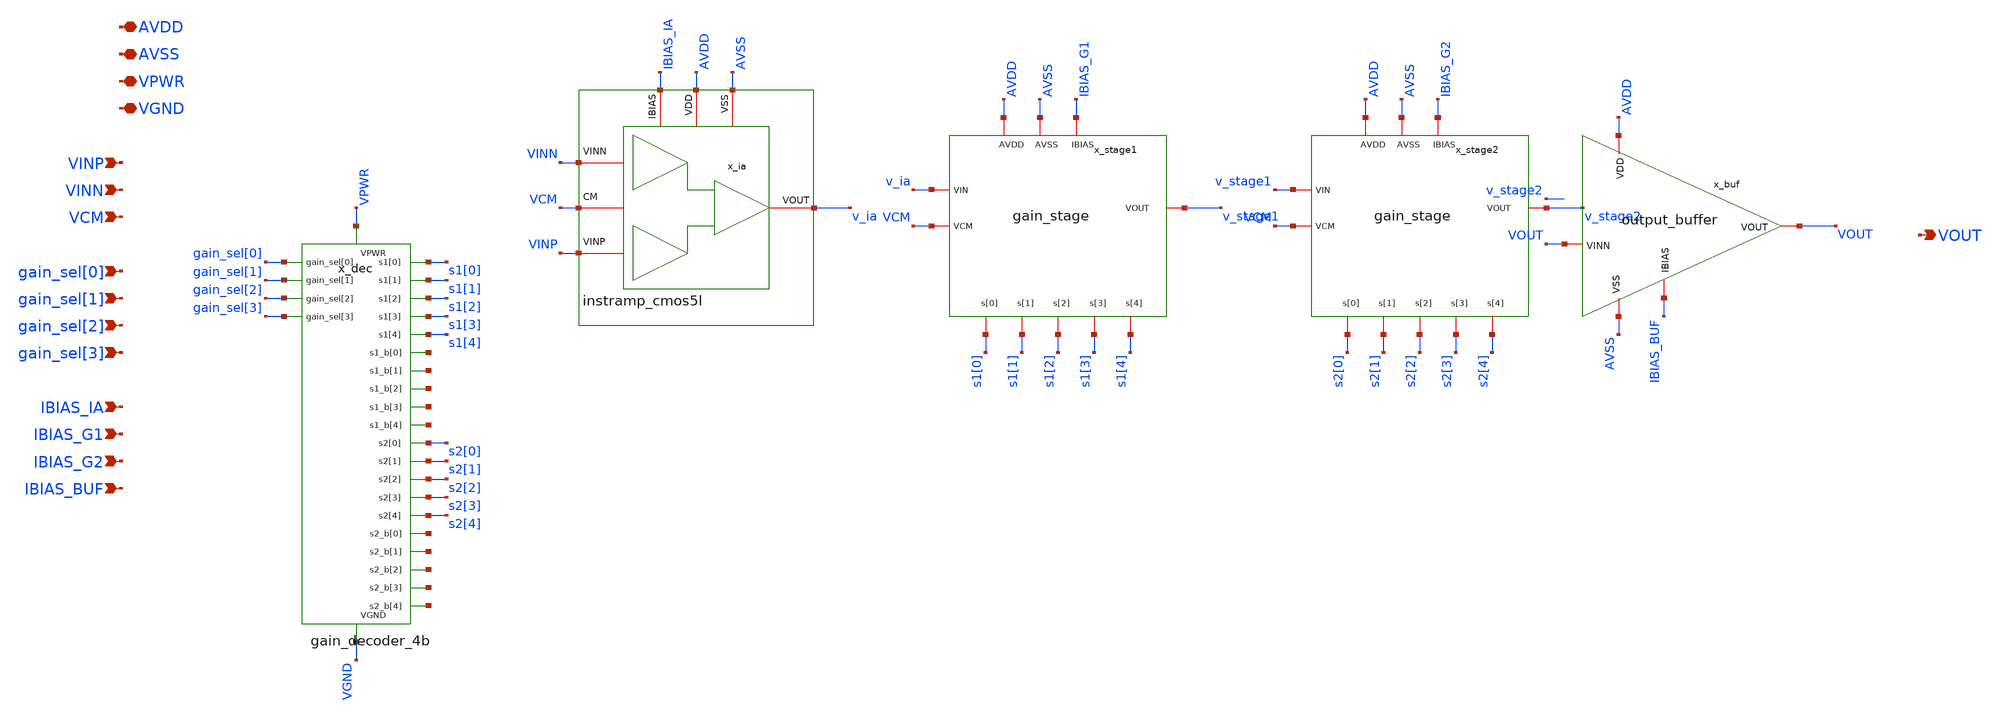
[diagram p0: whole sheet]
** sch_path: xschem/pgia_top/pgia_top.sch
**.subckt pgia_top AVDD AVSS VPWR VGND VINP VINN VCM gain_sel[0] gain_sel[1] gain_sel[2] gain_sel[3]
*+ IBIAS_IA IBIAS_G1 IBIAS_G2 IBIAS_BUF VOUT
*.iopin AVDD
*.iopin AVSS
*.iopin VPWR
*.iopin VGND
*.ipin VINP
*.ipin VINN
*.ipin VCM
*.ipin gain_sel[0]
*.ipin gain_sel[1]
*.ipin gain_sel[2]
*.ipin gain_sel[3]
*.ipin IBIAS_IA
*.ipin IBIAS_G1
*.ipin IBIAS_G2
*.ipin IBIAS_BUF
*.opin VOUT
x_dec VGND VPWR gain_sel[0] gain_sel[1] gain_sel[2] gain_sel[3] s1[0] s1[1] s1[2] s1[3] s1[4] net1
+ net2 net3 net4 net5 s2[0] s2[1] s2[2] s2[3] s2[4] net6 net7 net8 net9 net10 gain_decoder_4b
x_ia AVSS AVDD IBIAS_IA VINN v_ia VINP VCM instramp_cmos5l
x_stage1 AVDD AVSS IBIAS_G1 v_ia VCM v_stage1 s1[0] s1[1] s1[2] s1[3] s1[4] gain_stage
x_stage2 AVDD AVSS IBIAS_G2 v_stage1 VCM v_stage2 s2[0] s2[1] s2[2] s2[3] s2[4] gain_stage
x_buf AVDD AVSS IBIAS_BUF VOUT VOUT output_buffer
**.ends
.end
